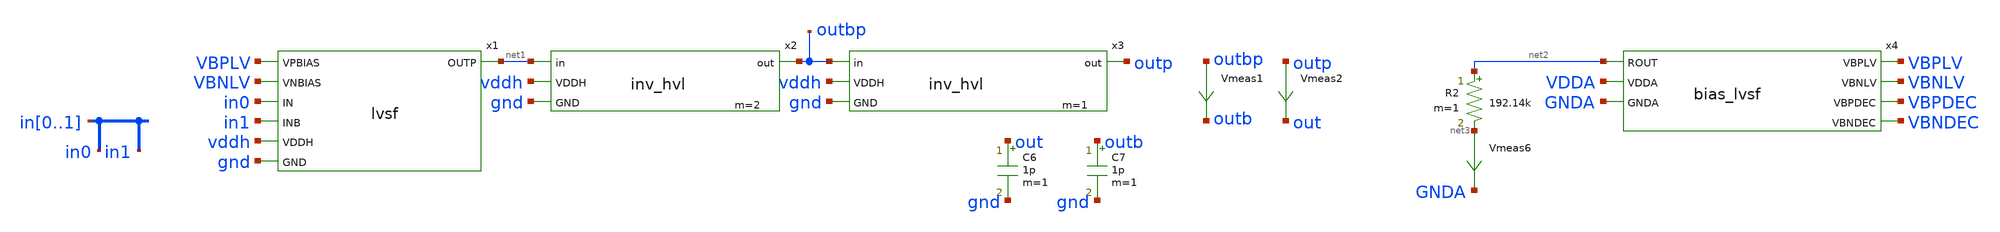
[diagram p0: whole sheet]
** sch_path: xschem/lvsf-tb.sch
.lib $::SKYWATER_MODELS/sky130.lib.spice tt
.include $::SKYWATER_STDCELLS/sky130_fd_sc_hd.spice

**.subckt lvsf-tb
x1 VBPLV VBNLV in0 in1 net1 vddh gnd lvsf
C6 out gnd 1p m=1
C7 outb gnd 1p m=1
Vmeas1 outbp outb 0
.save i(vmeas1)
Vmeas2 outp out 0
.save i(vmeas2)
x2 net1 outbp vddh gnd inv_hvl m=2
x3 outbp outp vddh gnd inv_hvl m=1
R2 net2 net3 192.14k m=1
Vmeas6 net3 GNDA 0
.save i(vmeas6)
x4 net2 VBPLV VBNLV VBPDEC VBNDEC VDDA GNDA bias_lvsf
**** begin user architecture code



  .param max_freq=100e3 period={1/max_freq} time_high={period/2}
  .param delay_vin1={time_high} delay_vin2={time_high*1.5}
  .param lval=100u

  .option wnflag=1
  .option safecurrents

  Vddh vddh gnd dc 5.5
  Vin  in0  gnd pulse(0 1.8 {delay_vin1} 1p 1p {time_high} {period})
  Vinb in1 gnd pulse(1.8 0 {delay_vin1} 1p 1p {time_high} {period})
  *vin in gnd 1.8
  *vinb inb gnd 0
  *vpb vpbias gnd 1.3273
  *vpb vpbias gnd 3.6965
  *vnb vnbias gnd 1.354
  *vnb vnbias gnd 1.5
  .control
     reset
     save all
     tran 1n 25u
     *dc vnb 0 5.5 0.01
     write lvsf-tb.raw
     set wr_vecnames
     set wr_singlescale
     wrdata $THESIS_WS/simulations/lvsf-tb.txt in0 in1
     set appendwrite
*    quit 0
  .endc



**** end user architecture code
**.ends

* expanding   symbol:  lvsf.sym # of pins=7
** sym_path: xschem/lvsf.sym
** sch_path: xschem/lvsf.sch
.subckt lvsf VPBIAS VNBIAS IN INB OUTP VDDH GND
*.ipin IN
*.ipin INB
*.opin OUTP
*.ipin VDDH
*.ipin GND
*.ipin VPBIAS
*.ipin VNBIAS
XM13 n1 IN GND GND sky130_fd_pr__nfet_01v8 L=0.15 W=3 nf=1 ad='int((nf+1)/2) * W/nf * 0.29' as='int((nf+2)/2) * W/nf * 0.29'
+ pd='2*int((nf+1)/2) * (W/nf + 0.29)' ps='2*int((nf+2)/2) * (W/nf + 0.29)' nrd='0.29 / W' nrs='0.29 / W'
+ sa=0 sb=0 sd=0 mult=1 m=1
XM1 net2 VPBIAS VDDH VDDH sky130_fd_pr__pfet_g5v0d10v5 L=0.8 W=1 nf=1 ad='int((nf+1)/2) * W/nf * 0.29'
+ as='int((nf+2)/2) * W/nf * 0.29' pd='2*int((nf+1)/2) * (W/nf + 0.29)' ps='2*int((nf+2)/2) * (W/nf + 0.29)'
+ nrd='0.29 / W' nrs='0.29 / W' sa=0 sb=0 sd=0 mult=1 m=1
XM2 net1 VPBIAS VDDH VDDH sky130_fd_pr__pfet_g5v0d10v5 L=0.8 W=1 nf=1 ad='int((nf+1)/2) * W/nf * 0.29'
+ as='int((nf+2)/2) * W/nf * 0.29' pd='2*int((nf+1)/2) * (W/nf + 0.29)' ps='2*int((nf+2)/2) * (W/nf + 0.29)'
+ nrd='0.29 / W' nrs='0.29 / W' sa=0 sb=0 sd=0 mult=1 m=1
XM3 OUTPB OUTP net2 VDDH sky130_fd_pr__pfet_g5v0d10v5 L=0.8 W=1 nf=1 ad='int((nf+1)/2) * W/nf * 0.29'
+ as='int((nf+2)/2) * W/nf * 0.29' pd='2*int((nf+1)/2) * (W/nf + 0.29)' ps='2*int((nf+2)/2) * (W/nf + 0.29)'
+ nrd='0.29 / W' nrs='0.29 / W' sa=0 sb=0 sd=0 mult=1 m=1
XM4 OUTP OUTPB net1 VDDH sky130_fd_pr__pfet_g5v0d10v5 L=0.8 W=1 nf=1 ad='int((nf+1)/2) * W/nf * 0.29'
+ as='int((nf+2)/2) * W/nf * 0.29' pd='2*int((nf+1)/2) * (W/nf + 0.29)' ps='2*int((nf+2)/2) * (W/nf + 0.29)'
+ nrd='0.29 / W' nrs='0.29 / W' sa=0 sb=0 sd=0 mult=1 m=1
XM5 OUTPB VNBIAS n1 GND sky130_fd_pr__nfet_g5v0d10v5 L=1 W=1 nf=1 ad='int((nf+1)/2) * W/nf * 0.29' as='int((nf+2)/2) * W/nf * 0.29'
+ pd='2*int((nf+1)/2) * (W/nf + 0.29)' ps='2*int((nf+2)/2) * (W/nf + 0.29)' nrd='0.29 / W' nrs='0.29 / W'
+ sa=0 sb=0 sd=0 mult=1 m=1
XM6 OUTP VNBIAS n2 GND sky130_fd_pr__nfet_g5v0d10v5 L=1 W=1 nf=1 ad='int((nf+1)/2) * W/nf * 0.29' as='int((nf+2)/2) * W/nf * 0.29'
+ pd='2*int((nf+1)/2) * (W/nf + 0.29)' ps='2*int((nf+2)/2) * (W/nf + 0.29)' nrd='0.29 / W' nrs='0.29 / W'
+ sa=0 sb=0 sd=0 mult=1 m=1
XM7 n2 INB GND GND sky130_fd_pr__nfet_01v8 L=0.15 W=3 nf=1 ad='int((nf+1)/2) * W/nf * 0.29' as='int((nf+2)/2) * W/nf * 0.29'
+ pd='2*int((nf+1)/2) * (W/nf + 0.29)' ps='2*int((nf+2)/2) * (W/nf + 0.29)' nrd='0.29 / W' nrs='0.29 / W'
+ sa=0 sb=0 sd=0 mult=1 m=1
.ends


* expanding   symbol:  inv_hvl.sym # of pins=4
** sym_path: xschem/inv_hvl.sym
** sch_path: xschem/inv_hvl.sch
.subckt inv_hvl in out VDDH GND
*.opin out
*.ipin VDDH
*.ipin GND
*.ipin in
.param wp=0.84 wn=0.42 l=0.5
XM1 out in VDDH VDDH sky130_fd_pr__pfet_g5v0d10v5 L=l W=wp nf=1 ad='int((nf+1)/2) * W/nf * 0.29' as='int((nf+2)/2) * W/nf * 0.29'
+ pd='2*int((nf+1)/2) * (W/nf + 0.29)' ps='2*int((nf+2)/2) * (W/nf + 0.29)' nrd='0.29 / W' nrs='0.29 / W'
+ sa=0 sb=0 sd=0 mult=mv m=mv
XM2 out in GND GND sky130_fd_pr__nfet_g5v0d10v5 L=l W=wn nf=1 ad='int((nf+1)/2) * W/nf * 0.29' as='int((nf+2)/2) * W/nf * 0.29'
+ pd='2*int((nf+1)/2) * (W/nf + 0.29)' ps='2*int((nf+2)/2) * (W/nf + 0.29)' nrd='0.29 / W' nrs='0.29 / W'
+ sa=0 sb=0 sd=0 mult=mv m=mv
.ends


* expanding   symbol:  bias_lvsf.sym # of pins=7
** sym_path: xschem/bias_lvsf.sym
** sch_path: xschem/bias_lvsf.sch
.subckt bias_lvsf ROUT VBPLV VBNLV VBPDEC VBNDEC VDDA GNDA
*.ipin ROUT
*.opin VBPLV
*.opin VBNLV
*.opin VBPDEC
*.opin VBNDEC
*.ipin VDDA
*.ipin GNDA
XM1 n1 n1 VDDA VDDA sky130_fd_pr__pfet_g5v0d10v5 L=lref W=wp_iref nf=1 ad='int((nf+1)/2) * W/nf * 0.29'
+ as='int((nf+2)/2) * W/nf * 0.29' pd='2*int((nf+1)/2) * (W/nf + 0.29)' ps='2*int((nf+2)/2) * (W/nf + 0.29)'
+ nrd='0.29 / W' nrs='0.29 / W' sa=0 sb=0 sd=0 mult=miref m=miref
.param wp_iref=1.8 wn_iref=0.6 miref=2 lref=4 lr=20
XM2 n2 n2 n1 VDDA sky130_fd_pr__pfet_g5v0d10v5 L=lref W=wp_iref nf=1 ad='int((nf+1)/2) * W/nf * 0.29'
+ as='int((nf+2)/2) * W/nf * 0.29' pd='2*int((nf+1)/2) * (W/nf + 0.29)' ps='2*int((nf+2)/2) * (W/nf + 0.29)'
+ nrd='0.29 / W' nrs='0.29 / W' sa=0 sb=0 sd=0 mult=miref m=miref
XR1 ROUT net1 GNDA sky130_fd_pr__res_xhigh_po_5p73 L=0.573 mult=1 m=1
XM3 net2 net1 n2 VDDA sky130_fd_pr__pfet_g5v0d10v5 L=lr W=wp_iref nf=1 ad='int((nf+1)/2) * W/nf * 0.29'
+ as='int((nf+2)/2) * W/nf * 0.29' pd='2*int((nf+1)/2) * (W/nf + 0.29)' ps='2*int((nf+2)/2) * (W/nf + 0.29)'
+ nrd='0.29 / W' nrs='0.29 / W' sa=0 sb=0 sd=0 mult=miref m=miref
XM4 net1 net1 net2 VDDA sky130_fd_pr__pfet_g5v0d10v5 L=lr W=wp_iref nf=1 ad='int((nf+1)/2) * W/nf * 0.29'
+ as='int((nf+2)/2) * W/nf * 0.29' pd='2*int((nf+1)/2) * (W/nf + 0.29)' ps='2*int((nf+2)/2) * (W/nf + 0.29)'
+ nrd='0.29 / W' nrs='0.29 / W' sa=0 sb=0 sd=0 mult=miref m=miref
XM5 net3 n1 VDDA VDDA sky130_fd_pr__pfet_g5v0d10v5 L=lref W=wp_iref nf=1 ad='int((nf+1)/2) * W/nf * 0.29'
+ as='int((nf+2)/2) * W/nf * 0.29' pd='2*int((nf+1)/2) * (W/nf + 0.29)' ps='2*int((nf+2)/2) * (W/nf + 0.29)'
+ nrd='0.29 / W' nrs='0.29 / W' sa=0 sb=0 sd=0 mult=miref m=miref
XM6 n3 n2 net3 VDDA sky130_fd_pr__pfet_g5v0d10v5 L=lref W=wp_iref nf=1 ad='int((nf+1)/2) * W/nf * 0.29'
+ as='int((nf+2)/2) * W/nf * 0.29' pd='2*int((nf+1)/2) * (W/nf + 0.29)' ps='2*int((nf+2)/2) * (W/nf + 0.29)'
+ nrd='0.29 / W' nrs='0.29 / W' sa=0 sb=0 sd=0 mult=miref m=miref
Vmeas1 net8 GNDA 0
.save i(vmeas1)
XM7 n3 n3 n4 GNDA sky130_fd_pr__nfet_g5v0d10v5 L=lref W=wn_iref nf=1 ad='int((nf+1)/2) * W/nf * 0.29'
+ as='int((nf+2)/2) * W/nf * 0.29' pd='2*int((nf+1)/2) * (W/nf + 0.29)' ps='2*int((nf+2)/2) * (W/nf + 0.29)'
+ nrd='0.29 / W' nrs='0.29 / W' sa=0 sb=0 sd=0 mult=miref m=miref
XM8 n4 n4 net8 GNDA sky130_fd_pr__nfet_g5v0d10v5 L=lref W=wn_iref nf=1 ad='int((nf+1)/2) * W/nf * 0.29'
+ as='int((nf+2)/2) * W/nf * 0.29' pd='2*int((nf+1)/2) * (W/nf + 0.29)' ps='2*int((nf+2)/2) * (W/nf + 0.29)'
+ nrd='0.29 / W' nrs='0.29 / W' sa=0 sb=0 sd=0 mult=miref m=miref
XM9 net4 n1 VDDA VDDA sky130_fd_pr__pfet_g5v0d10v5 L=lref W=wp_iref nf=1 ad='int((nf+1)/2) * W/nf * 0.29'
+ as='int((nf+2)/2) * W/nf * 0.29' pd='2*int((nf+1)/2) * (W/nf + 0.29)' ps='2*int((nf+2)/2) * (W/nf + 0.29)'
+ nrd='0.29 / W' nrs='0.29 / W' sa=0 sb=0 sd=0 mult=miref m=miref
XM10 VBNLV n2 net4 VDDA sky130_fd_pr__pfet_g5v0d10v5 L=lref W=wp_iref nf=1 ad='int((nf+1)/2) * W/nf * 0.29'
+ as='int((nf+2)/2) * W/nf * 0.29' pd='2*int((nf+1)/2) * (W/nf + 0.29)' ps='2*int((nf+2)/2) * (W/nf + 0.29)'
+ nrd='0.29 / W' nrs='0.29 / W' sa=0 sb=0 sd=0 mult=miref m=miref
XM11 net5 n1 VDDA VDDA sky130_fd_pr__pfet_g5v0d10v5 L=lref W=wp_iref nf=1 ad='int((nf+1)/2) * W/nf * 0.29'
+ as='int((nf+2)/2) * W/nf * 0.29' pd='2*int((nf+1)/2) * (W/nf + 0.29)' ps='2*int((nf+2)/2) * (W/nf + 0.29)'
+ nrd='0.29 / W' nrs='0.29 / W' sa=0 sb=0 sd=0 mult=miref m=miref
XM12 VBNDEC n2 net5 VDDA sky130_fd_pr__pfet_g5v0d10v5 L=lref W=wp_iref nf=1 ad='int((nf+1)/2) * W/nf * 0.29'
+ as='int((nf+2)/2) * W/nf * 0.29' pd='2*int((nf+1)/2) * (W/nf + 0.29)' ps='2*int((nf+2)/2) * (W/nf + 0.29)'
+ nrd='0.29 / W' nrs='0.29 / W' sa=0 sb=0 sd=0 mult=miref m=miref
XM13 VBNLV VBNLV n6 GNDA sky130_fd_pr__nfet_g5v0d10v5 L=lref W=wn_iref nf=1 ad='int((nf+1)/2) * W/nf * 0.29'
+ as='int((nf+2)/2) * W/nf * 0.29' pd='2*int((nf+1)/2) * (W/nf + 0.29)' ps='2*int((nf+2)/2) * (W/nf + 0.29)'
+ nrd='0.29 / W' nrs='0.29 / W' sa=0 sb=0 sd=0 mult=miref m=miref
XM14 n6 VBNLV net9 GNDA sky130_fd_pr__nfet_g5v0d10v5 L=5.3 W=0.6 nf=1 ad='int((nf+1)/2) * W/nf * 0.29'
+ as='int((nf+2)/2) * W/nf * 0.29' pd='2*int((nf+1)/2) * (W/nf + 0.29)' ps='2*int((nf+2)/2) * (W/nf + 0.29)'
+ nrd='0.29 / W' nrs='0.29 / W' sa=0 sb=0 sd=0 mult=1 m=1
Vmeas2 net9 GNDA 0
.save i(vmeas2)
XM15 VBNDEC VBNDEC n7 GNDA sky130_fd_pr__nfet_g5v0d10v5 L=lref W=wn_iref nf=1 ad='int((nf+1)/2) * W/nf * 0.29'
+ as='int((nf+2)/2) * W/nf * 0.29' pd='2*int((nf+1)/2) * (W/nf + 0.29)' ps='2*int((nf+2)/2) * (W/nf + 0.29)'
+ nrd='0.29 / W' nrs='0.29 / W' sa=0 sb=0 sd=0 mult=miref m=miref
XM16 n7 VBNDEC net10 GNDA sky130_fd_pr__nfet_g5v0d10v5 L=9.7 W=0.61 nf=1 ad='int((nf+1)/2) * W/nf * 0.29'
+ as='int((nf+2)/2) * W/nf * 0.29' pd='2*int((nf+1)/2) * (W/nf + 0.29)' ps='2*int((nf+2)/2) * (W/nf + 0.29)'
+ nrd='0.29 / W' nrs='0.29 / W' sa=0 sb=0 sd=0 mult=1 m=1
Vmeas3 net10 GNDA 0
.save i(vmeas3)
XM17 n10 VBPLV VDDA VDDA sky130_fd_pr__pfet_g5v0d10v5 L=9.2 W=1 nf=1 ad='int((nf+1)/2) * W/nf * 0.29'
+ as='int((nf+2)/2) * W/nf * 0.29' pd='2*int((nf+1)/2) * (W/nf + 0.29)' ps='2*int((nf+2)/2) * (W/nf + 0.29)'
+ nrd='0.29 / W' nrs='0.29 / W' sa=0 sb=0 sd=0 mult=1 m=1
XM18 VBPLV VBPLV n10 VDDA sky130_fd_pr__pfet_g5v0d10v5 L=lref W=wp_iref nf=1 ad='int((nf+1)/2) * W/nf * 0.29'
+ as='int((nf+2)/2) * W/nf * 0.29' pd='2*int((nf+1)/2) * (W/nf + 0.29)' ps='2*int((nf+2)/2) * (W/nf + 0.29)'
+ nrd='0.29 / W' nrs='0.29 / W' sa=0 sb=0 sd=0 mult=miref m=miref
Vmeas4 net11 GNDA 0
.save i(vmeas4)
XM19 VBPLV n3 net6 GNDA sky130_fd_pr__nfet_g5v0d10v5 L=lref W=wn_iref nf=1 ad='int((nf+1)/2) * W/nf * 0.29'
+ as='int((nf+2)/2) * W/nf * 0.29' pd='2*int((nf+1)/2) * (W/nf + 0.29)' ps='2*int((nf+2)/2) * (W/nf + 0.29)'
+ nrd='0.29 / W' nrs='0.29 / W' sa=0 sb=0 sd=0 mult=miref m=miref
XM20 net6 n4 net11 GNDA sky130_fd_pr__nfet_g5v0d10v5 L=lref W=wn_iref nf=1 ad='int((nf+1)/2) * W/nf * 0.29'
+ as='int((nf+2)/2) * W/nf * 0.29' pd='2*int((nf+1)/2) * (W/nf + 0.29)' ps='2*int((nf+2)/2) * (W/nf + 0.29)'
+ nrd='0.29 / W' nrs='0.29 / W' sa=0 sb=0 sd=0 mult=miref m=miref
XM26 net7 n1 VDDA VDDA sky130_fd_pr__pfet_g5v0d10v5 L=lref W=wp_iref nf=1 ad='int((nf+1)/2) * W/nf * 0.29'
+ as='int((nf+2)/2) * W/nf * 0.29' pd='2*int((nf+1)/2) * (W/nf + 0.29)' ps='2*int((nf+2)/2) * (W/nf + 0.29)'
+ nrd='0.29 / W' nrs='0.29 / W' sa=0 sb=0 sd=0 mult=miref m=miref
XM27 VBPDEC n2 net7 VDDA sky130_fd_pr__pfet_g5v0d10v5 L=lref W=wp_iref nf=1 ad='int((nf+1)/2) * W/nf * 0.29'
+ as='int((nf+2)/2) * W/nf * 0.29' pd='2*int((nf+1)/2) * (W/nf + 0.29)' ps='2*int((nf+2)/2) * (W/nf + 0.29)'
+ nrd='0.29 / W' nrs='0.29 / W' sa=0 sb=0 sd=0 mult=miref m=miref
XM28 VBPDEC VBPDEC n14 GNDA sky130_fd_pr__nfet_g5v0d10v5 L=lref W=wn_iref nf=1 ad='int((nf+1)/2) * W/nf * 0.29'
+ as='int((nf+2)/2) * W/nf * 0.29' pd='2*int((nf+1)/2) * (W/nf + 0.29)' ps='2*int((nf+2)/2) * (W/nf + 0.29)'
+ nrd='0.29 / W' nrs='0.29 / W' sa=0 sb=0 sd=0 mult=miref m=miref
XM29 n14 n14 net12 GNDA sky130_fd_pr__nfet_g5v0d10v5 L=12 W=0.64 nf=1 ad='int((nf+1)/2) * W/nf * 0.29'
+ as='int((nf+2)/2) * W/nf * 0.29' pd='2*int((nf+1)/2) * (W/nf + 0.29)' ps='2*int((nf+2)/2) * (W/nf + 0.29)'
+ nrd='0.29 / W' nrs='0.29 / W' sa=0 sb=0 sd=0 mult=1 m=1
Vmeas6 net12 GNDA 0
.save i(vmeas6)
.ends

.end
